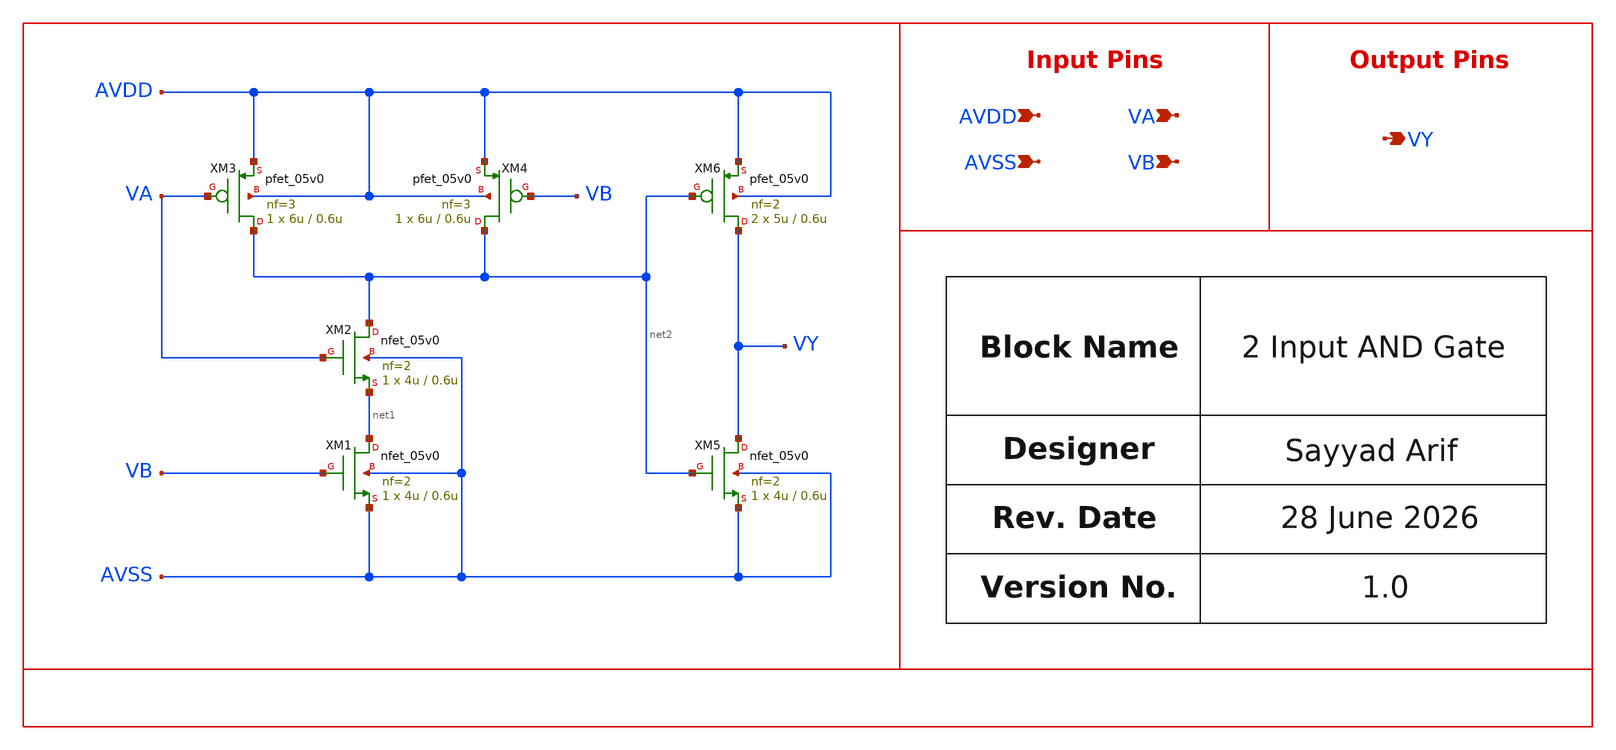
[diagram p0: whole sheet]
** sch_path: design/schematics/ADC/DSM_Loop_filter/First_int/AND_gate/sa_cic_bms_afe_iadc_first_int_and2.sch
**.subckt sa_cic_bms_afe_iadc_first_int_and2 VA VB AVDD AVSS VY
*.ipin VA
*.ipin VB
*.ipin AVDD
*.ipin AVSS
*.opin VY
XM1 net1 VB AVSS AVSS nfet_05v0 L=0.6u W=4u nf=2 ad='int((nf+1)/2) * W/nf * 0.18u' as='int((nf+2)/2) * W/nf * 0.18u'
+ pd='2*int((nf+1)/2) * (W/nf + 0.18u)' ps='2*int((nf+2)/2) * (W/nf + 0.18u)' nrd='0.18u / W' nrs='0.18u / W'
+ sa=0 sb=0 sd=0 m=1
XM3 net2 VA AVDD AVDD pfet_05v0 L=0.6u W=6u nf=3 ad='int((nf+1)/2) * W/nf * 0.18u' as='int((nf+2)/2) * W/nf * 0.18u'
+ pd='2*int((nf+1)/2) * (W/nf + 0.18u)' ps='2*int((nf+2)/2) * (W/nf + 0.18u)' nrd='0.18u / W' nrs='0.18u / W'
+ sa=0 sb=0 sd=0 m=1
XM2 net2 VA net1 AVSS nfet_05v0 L=0.6u W=4u nf=2 ad='int((nf+1)/2) * W/nf * 0.18u' as='int((nf+2)/2) * W/nf * 0.18u'
+ pd='2*int((nf+1)/2) * (W/nf + 0.18u)' ps='2*int((nf+2)/2) * (W/nf + 0.18u)' nrd='0.18u / W' nrs='0.18u / W'
+ sa=0 sb=0 sd=0 m=1
XM4 net2 VB AVDD AVDD pfet_05v0 L=0.6u W=6u nf=3 ad='int((nf+1)/2) * W/nf * 0.18u' as='int((nf+2)/2) * W/nf * 0.18u'
+ pd='2*int((nf+1)/2) * (W/nf + 0.18u)' ps='2*int((nf+2)/2) * (W/nf + 0.18u)' nrd='0.18u / W' nrs='0.18u / W'
+ sa=0 sb=0 sd=0 m=1
XM5 VY net2 AVSS AVSS nfet_05v0 L=0.6u W=4u nf=2 ad='int((nf+1)/2) * W/nf * 0.18u' as='int((nf+2)/2) * W/nf * 0.18u'
+ pd='2*int((nf+1)/2) * (W/nf + 0.18u)' ps='2*int((nf+2)/2) * (W/nf + 0.18u)' nrd='0.18u / W' nrs='0.18u / W'
+ sa=0 sb=0 sd=0 m=1
XM6 VY net2 AVDD AVDD pfet_05v0 L=0.6u W=5u nf=2 ad='int((nf+1)/2) * W/nf * 0.18u' as='int((nf+2)/2) * W/nf * 0.18u'
+ pd='2*int((nf+1)/2) * (W/nf + 0.18u)' ps='2*int((nf+2)/2) * (W/nf + 0.18u)' nrd='0.18u / W' nrs='0.18u / W'
+ sa=0 sb=0 sd=0 m=2
**.ends
.end
